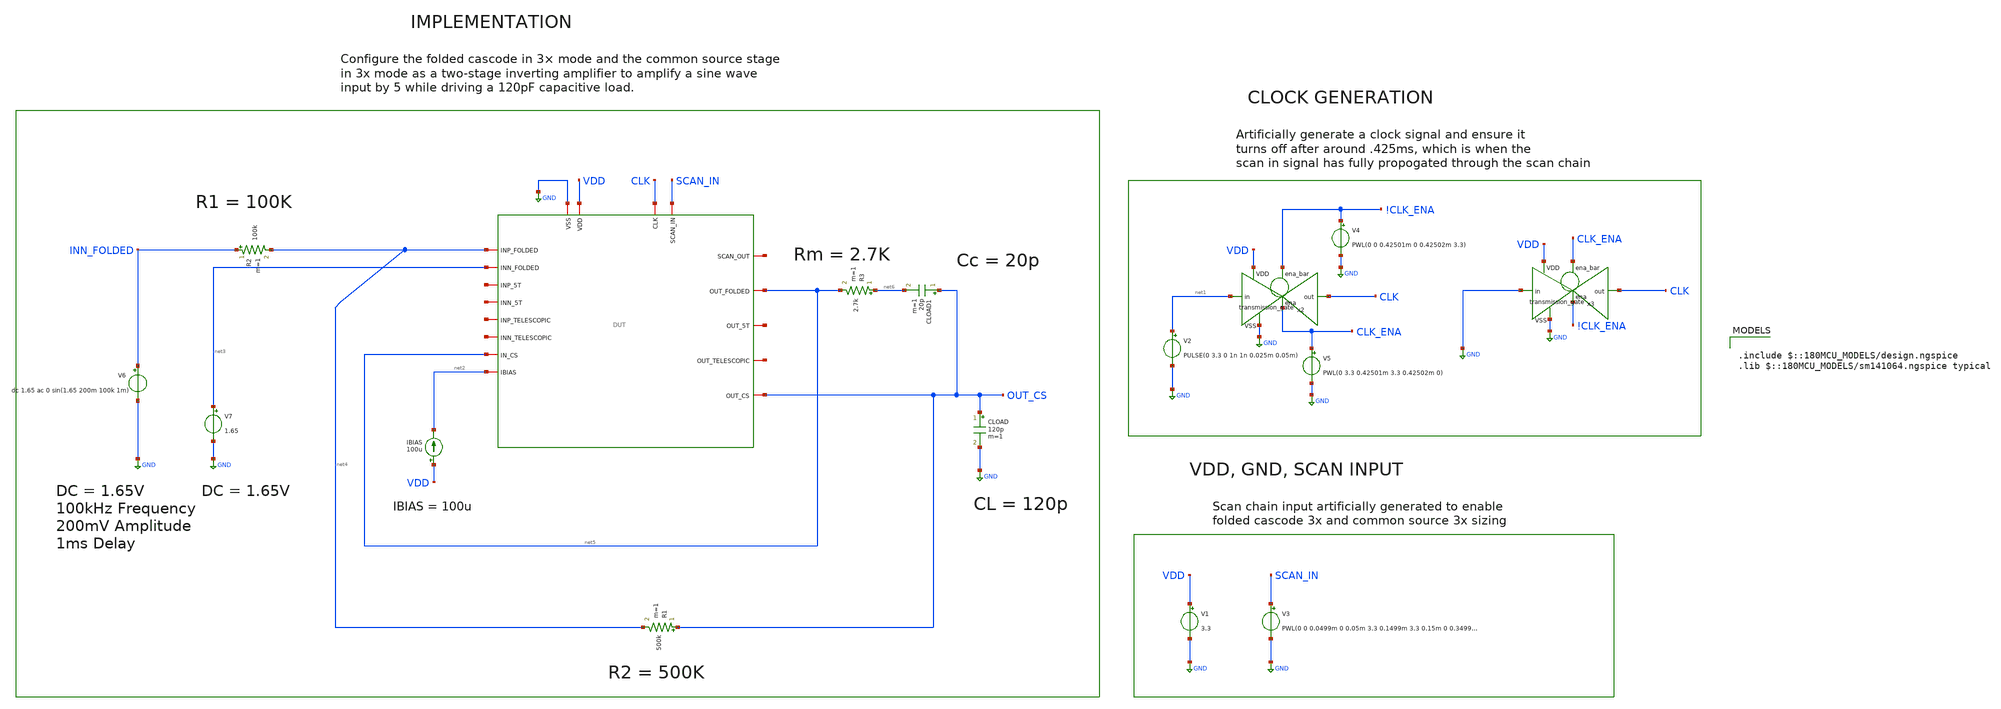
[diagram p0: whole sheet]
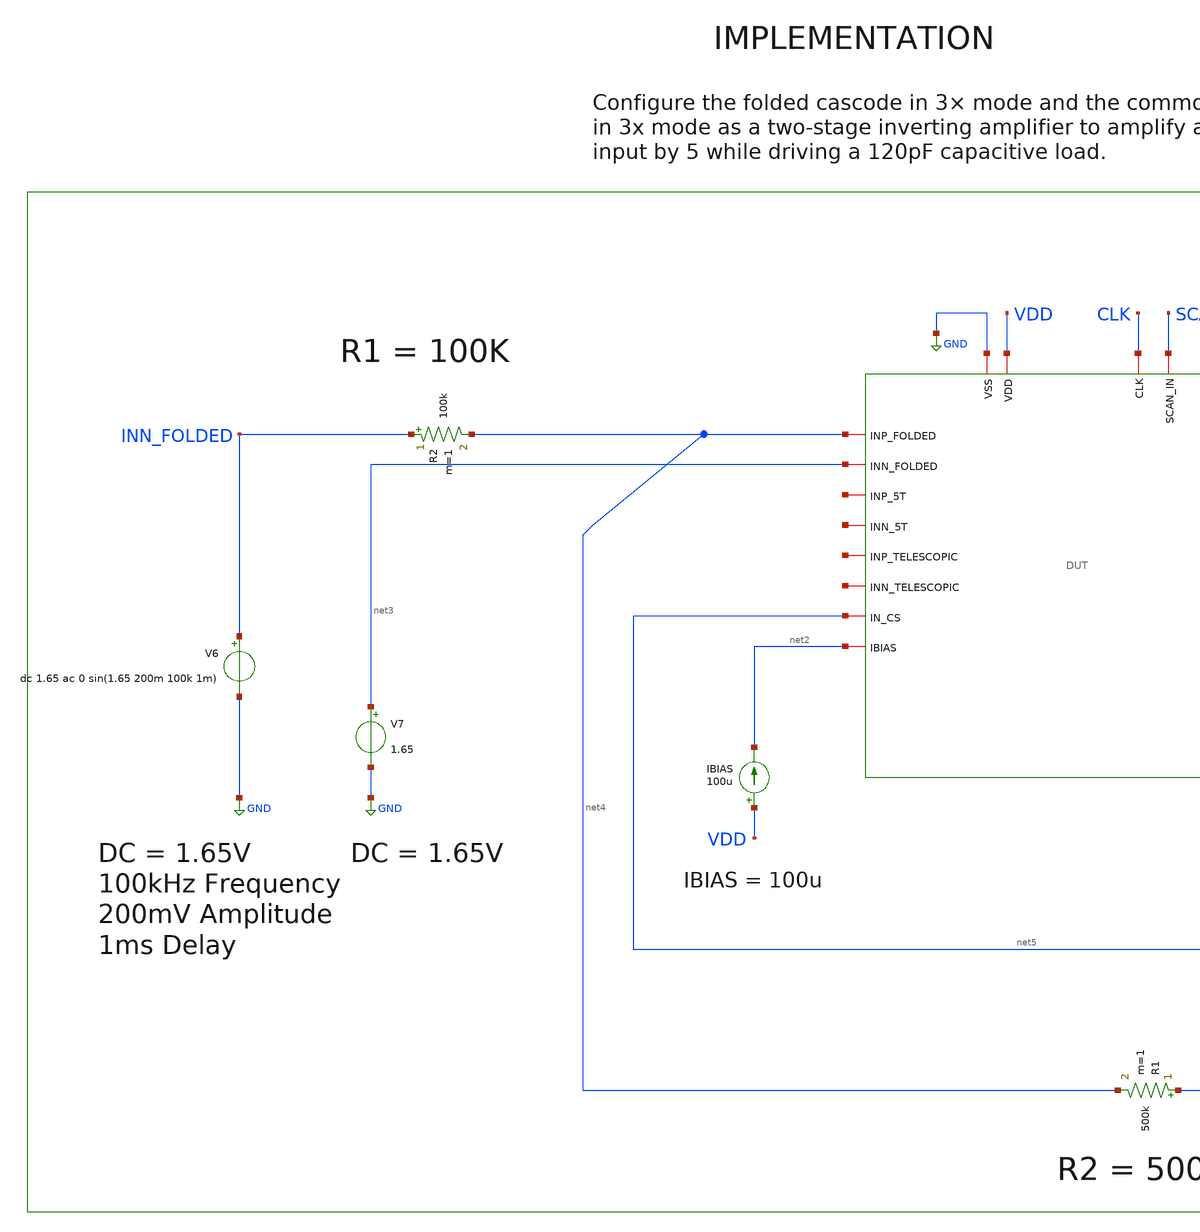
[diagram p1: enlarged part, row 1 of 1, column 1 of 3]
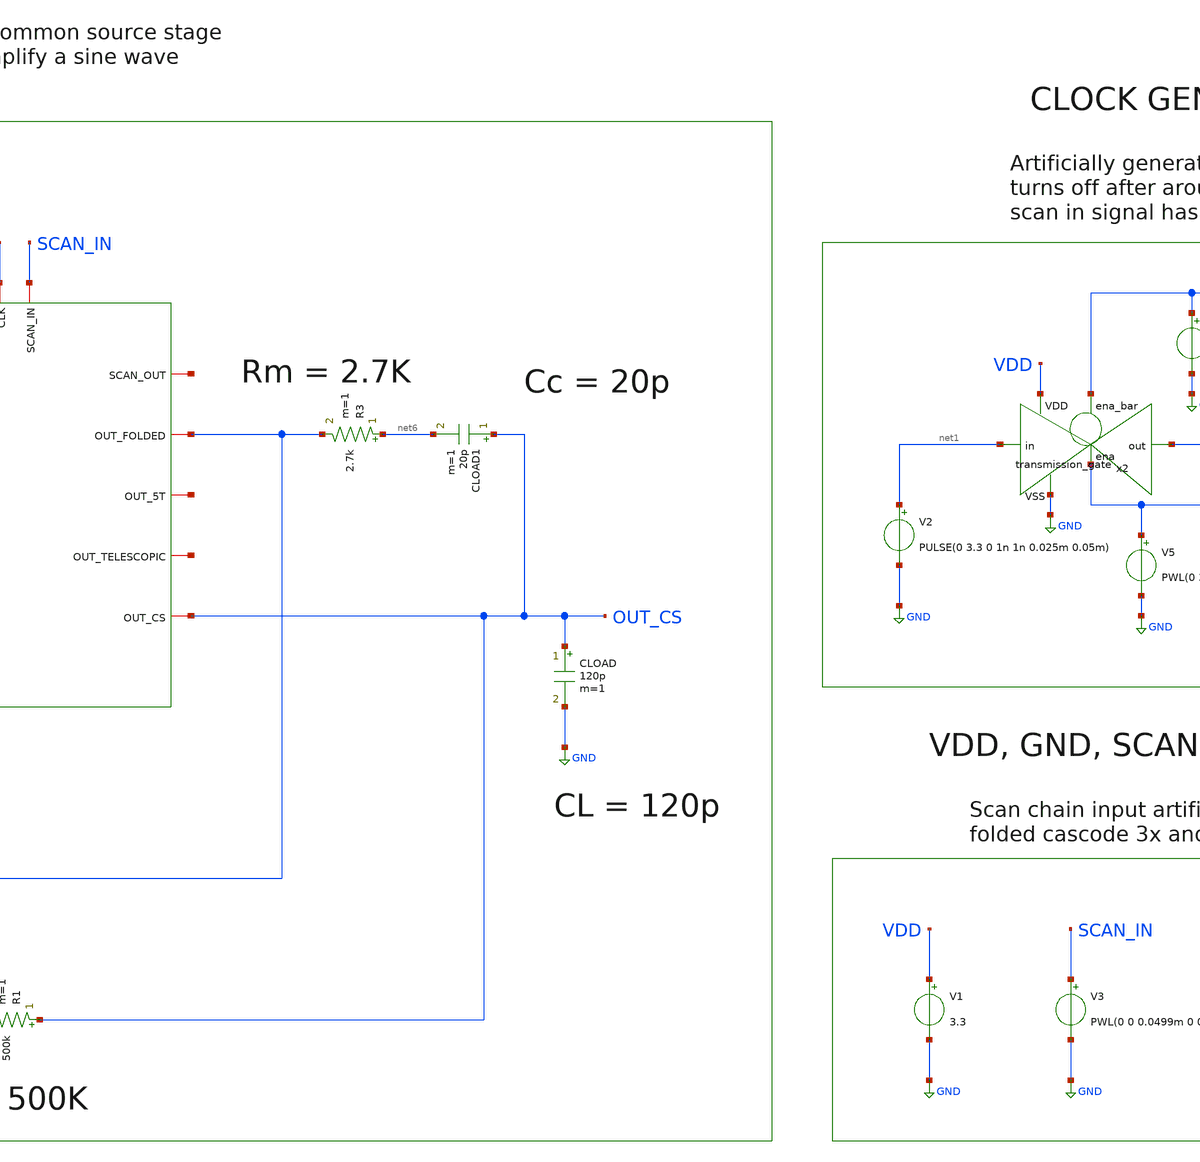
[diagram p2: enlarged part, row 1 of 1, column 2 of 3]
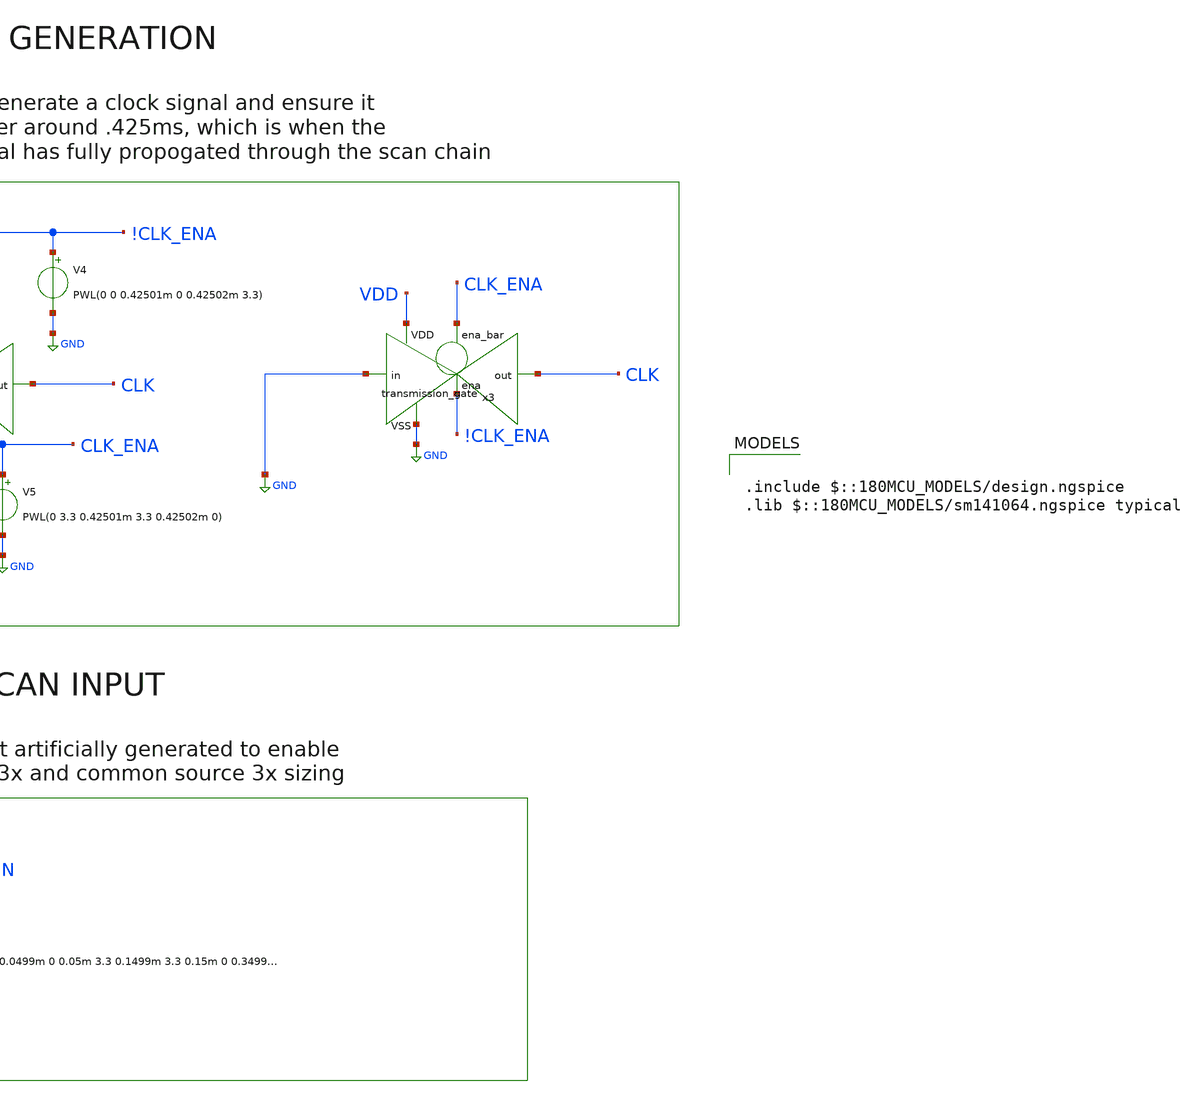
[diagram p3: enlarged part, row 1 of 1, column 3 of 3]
** sch_path: designs/libs/old_files/old_top_level/etj/ota_folded/two_stage/inverting_amp_3x.sch
**.subckt inverting_amp_3x
V3 SCAN_IN GND PWL(0 0 0.0499m 0 0.05m 3.3 0.1499m 3.3 0.15m 0 0.34999m 0 0.35m 3.3 0.499999m 3.3
+ 0.5m 0)
V1 VDD GND 3.3
V2 net1 GND PULSE(0 3.3 0 1n 1n 0.025m 0.05m)
x2 !CLK_ENA VDD CLK net1 GND CLK_ENA transmission_gate
V4 !CLK_ENA GND PWL(0 0 0.42501m 0 0.42502m 3.3)
V5 CLK_ENA GND PWL(0 3.3 0.42501m 3.3 0.42502m 0)
IBIAS VDD net2 100u
CLOAD OUT_CS GND 120p m=1
R3 net6 net5 2.7k m=1
CLOAD1 OUT_CS net6 20p m=1
V7 net3 GND 1.65
R2 INN_FOLDED net4 100k m=1
R1 OUT_CS net4 500k m=1
V6 INN_FOLDED GND dc 1.65 ac 0 sin(1.65 200m 100k 1m)
x3 CLK_ENA VDD CLK GND GND !CLK_ENA transmission_gate
x1 CLK net7 SCAN_IN GND VDD net5 net4 net8 net2 net3 net9 net10 net11 net12 OUT_CS net5 net13 DUT
**** begin user architecture code

.include $::180MCU_MODELS/design.ngspice
.lib $::180MCU_MODELS/sm141064.ngspice typical



.control
set color0 = white
set color1 = black
tran .01u 3m

meas tran en0_folded find v(x1.en_0_folded) at=5m
meas tran enb0_folded find v(x1.!en_0_folded) at=5m
meas tran en1_folded find v(x1.en_1_folded) at=5m
meas tran enb1_folded find v(x1.!en_1_folded) at=5m
meas tran en0_cs find v(x1.en_0_cs) at=5m
meas tran enb0_cs find v(x1.!en_0_cs) at=5m
meas tran en1_cs find v(x1.en_1_cs) at=5m
meas tran enb1_cs find v(x1.!en_1_cs) at=5m
print en0_folded enb0_folded en1_folded enb1_folded
print en0_cs enb0_cs en1_cs enb1_cs

plot v(OUT_CS) v(INN_FOLDED)
meas tran vout_pp pp v(out_cs) from=5m to=10m
meas tran vin_pp pp v(inn_folded) from=5m to=10m
let gain = vout_pp / vin_pp
print gain

wrdata /foss/designs/libs/core_tb/etj/ota_folded/two_stage/txt_results/two_stage_tran_fine.txt
+ v(out_cs) v(inn_folded)

.endc


**** end user architecture code
**.ends
.GLOBAL GND
.end
